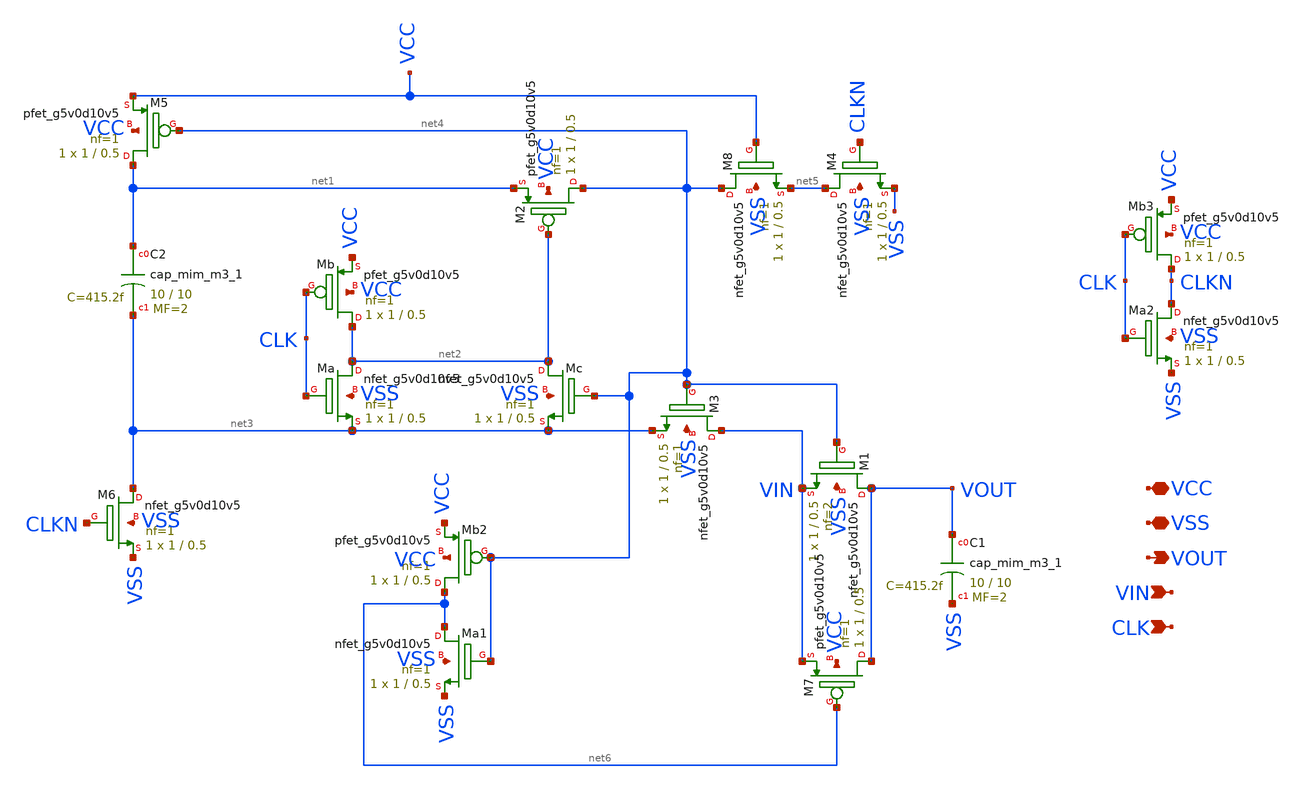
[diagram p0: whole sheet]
** sch_path: sample_hold/schematic/sample_hold.sch
**.subckt sample_hold VCC VIN VOUT CLK VSS
*.iopin VCC
*.ipin VIN
*.opin VOUT
*.ipin CLK
*.iopin VSS
XM5 net1 net4 VCC VCC sky130_fd_pr__pfet_g5v0d10v5 L=0.5 W=1 nf=1 ad='int((nf+1)/2) * W/nf * 0.29' as='int((nf+2)/2) * W/nf * 0.29'
+ pd='2*int((nf+1)/2) * (W/nf + 0.29)' ps='2*int((nf+2)/2) * (W/nf + 0.29)' nrd='0.29 / W' nrs='0.29 / W'
+ sa=0 sb=0 sd=0 mult=1 m=1
XM6 net3 CLKN VSS VSS sky130_fd_pr__nfet_g5v0d10v5 L=0.5 W=1 nf=1 ad='int((nf+1)/2) * W/nf * 0.29' as='int((nf+2)/2) * W/nf * 0.29'
+ pd='2*int((nf+1)/2) * (W/nf + 0.29)' ps='2*int((nf+2)/2) * (W/nf + 0.29)' nrd='0.29 / W' nrs='0.29 / W'
+ sa=0 sb=0 sd=0 mult=1 m=1
XMa net2 CLK net3 VSS sky130_fd_pr__nfet_g5v0d10v5 L=0.5 W=1 nf=1 ad='int((nf+1)/2) * W/nf * 0.29' as='int((nf+2)/2) * W/nf * 0.29'
+ pd='2*int((nf+1)/2) * (W/nf + 0.29)' ps='2*int((nf+2)/2) * (W/nf + 0.29)' nrd='0.29 / W' nrs='0.29 / W'
+ sa=0 sb=0 sd=0 mult=1 m=1
XMb net2 CLK VCC VCC sky130_fd_pr__pfet_g5v0d10v5 L=0.5 W=1 nf=1 ad='int((nf+1)/2) * W/nf * 0.29' as='int((nf+2)/2) * W/nf * 0.29'
+ pd='2*int((nf+1)/2) * (W/nf + 0.29)' ps='2*int((nf+2)/2) * (W/nf + 0.29)' nrd='0.29 / W' nrs='0.29 / W'
+ sa=0 sb=0 sd=0 mult=1 m=1
XMc net2 net4 net3 VSS sky130_fd_pr__nfet_g5v0d10v5 L=0.5 W=1 nf=1 ad='int((nf+1)/2) * W/nf * 0.29' as='int((nf+2)/2) * W/nf * 0.29'
+ pd='2*int((nf+1)/2) * (W/nf + 0.29)' ps='2*int((nf+2)/2) * (W/nf + 0.29)' nrd='0.29 / W' nrs='0.29 / W'
+ sa=0 sb=0 sd=0 mult=1 m=1
XM2 net4 net2 net1 VCC sky130_fd_pr__pfet_g5v0d10v5 L=0.5 W=1 nf=1 ad='int((nf+1)/2) * W/nf * 0.29' as='int((nf+2)/2) * W/nf * 0.29'
+ pd='2*int((nf+1)/2) * (W/nf + 0.29)' ps='2*int((nf+2)/2) * (W/nf + 0.29)' nrd='0.29 / W' nrs='0.29 / W'
+ sa=0 sb=0 sd=0 mult=1 m=1
XM3 VIN net4 net3 VSS sky130_fd_pr__nfet_g5v0d10v5 L=0.5 W=1 nf=1 ad='int((nf+1)/2) * W/nf * 0.29' as='int((nf+2)/2) * W/nf * 0.29'
+ pd='2*int((nf+1)/2) * (W/nf + 0.29)' ps='2*int((nf+2)/2) * (W/nf + 0.29)' nrd='0.29 / W' nrs='0.29 / W'
+ sa=0 sb=0 sd=0 mult=1 m=1
XM8 net4 VCC net5 VSS sky130_fd_pr__nfet_g5v0d10v5 L=0.5 W=1 nf=1 ad='int((nf+1)/2) * W/nf * 0.29' as='int((nf+2)/2) * W/nf * 0.29'
+ pd='2*int((nf+1)/2) * (W/nf + 0.29)' ps='2*int((nf+2)/2) * (W/nf + 0.29)' nrd='0.29 / W' nrs='0.29 / W'
+ sa=0 sb=0 sd=0 mult=1 m=1
XM4 net5 CLKN VSS VSS sky130_fd_pr__nfet_g5v0d10v5 L=0.5 W=1 nf=1 ad='int((nf+1)/2) * W/nf * 0.29' as='int((nf+2)/2) * W/nf * 0.29'
+ pd='2*int((nf+1)/2) * (W/nf + 0.29)' ps='2*int((nf+2)/2) * (W/nf + 0.29)' nrd='0.29 / W' nrs='0.29 / W'
+ sa=0 sb=0 sd=0 mult=1 m=1
XM1 VOUT net4 VIN VSS sky130_fd_pr__nfet_g5v0d10v5 L=0.5 W=1 nf=2 ad='int((nf+1)/2) * W/nf * 0.29' as='int((nf+2)/2) * W/nf * 0.29'
+ pd='2*int((nf+1)/2) * (W/nf + 0.29)' ps='2*int((nf+2)/2) * (W/nf + 0.29)' nrd='0.29 / W' nrs='0.29 / W'
+ sa=0 sb=0 sd=0 mult=1 m=1
XM7 VOUT net6 VIN VCC sky130_fd_pr__pfet_g5v0d10v5 L=0.5 W=1 nf=1 ad='int((nf+1)/2) * W/nf * 0.29' as='int((nf+2)/2) * W/nf * 0.29'
+ pd='2*int((nf+1)/2) * (W/nf + 0.29)' ps='2*int((nf+2)/2) * (W/nf + 0.29)' nrd='0.29 / W' nrs='0.29 / W'
+ sa=0 sb=0 sd=0 mult=1 m=1
XMa1 net6 net4 VSS VSS sky130_fd_pr__nfet_g5v0d10v5 L=0.5 W=1 nf=1 ad='int((nf+1)/2) * W/nf * 0.29' as='int((nf+2)/2) * W/nf * 0.29'
+ pd='2*int((nf+1)/2) * (W/nf + 0.29)' ps='2*int((nf+2)/2) * (W/nf + 0.29)' nrd='0.29 / W' nrs='0.29 / W'
+ sa=0 sb=0 sd=0 mult=1 m=1
XMb2 net6 net4 VCC VCC sky130_fd_pr__pfet_g5v0d10v5 L=0.5 W=1 nf=1 ad='int((nf+1)/2) * W/nf * 0.29' as='int((nf+2)/2) * W/nf * 0.29'
+ pd='2*int((nf+1)/2) * (W/nf + 0.29)' ps='2*int((nf+2)/2) * (W/nf + 0.29)' nrd='0.29 / W' nrs='0.29 / W'
+ sa=0 sb=0 sd=0 mult=1 m=1
XC1 VOUT VSS sky130_fd_pr__cap_mim_m3_1 W=10 L=10 MF=2 m=2
XC2 net1 net3 sky130_fd_pr__cap_mim_m3_1 W=10 L=10 MF=2 m=2
XMa2 CLKN CLK VSS VSS sky130_fd_pr__nfet_g5v0d10v5 L=0.5 W=1 nf=1 ad='int((nf+1)/2) * W/nf * 0.29' as='int((nf+2)/2) * W/nf * 0.29'
+ pd='2*int((nf+1)/2) * (W/nf + 0.29)' ps='2*int((nf+2)/2) * (W/nf + 0.29)' nrd='0.29 / W' nrs='0.29 / W'
+ sa=0 sb=0 sd=0 mult=1 m=1
XMb3 CLKN CLK VCC VCC sky130_fd_pr__pfet_g5v0d10v5 L=0.5 W=1 nf=1 ad='int((nf+1)/2) * W/nf * 0.29' as='int((nf+2)/2) * W/nf * 0.29'
+ pd='2*int((nf+1)/2) * (W/nf + 0.29)' ps='2*int((nf+2)/2) * (W/nf + 0.29)' nrd='0.29 / W' nrs='0.29 / W'
+ sa=0 sb=0 sd=0 mult=1 m=1
**.ends
.end
